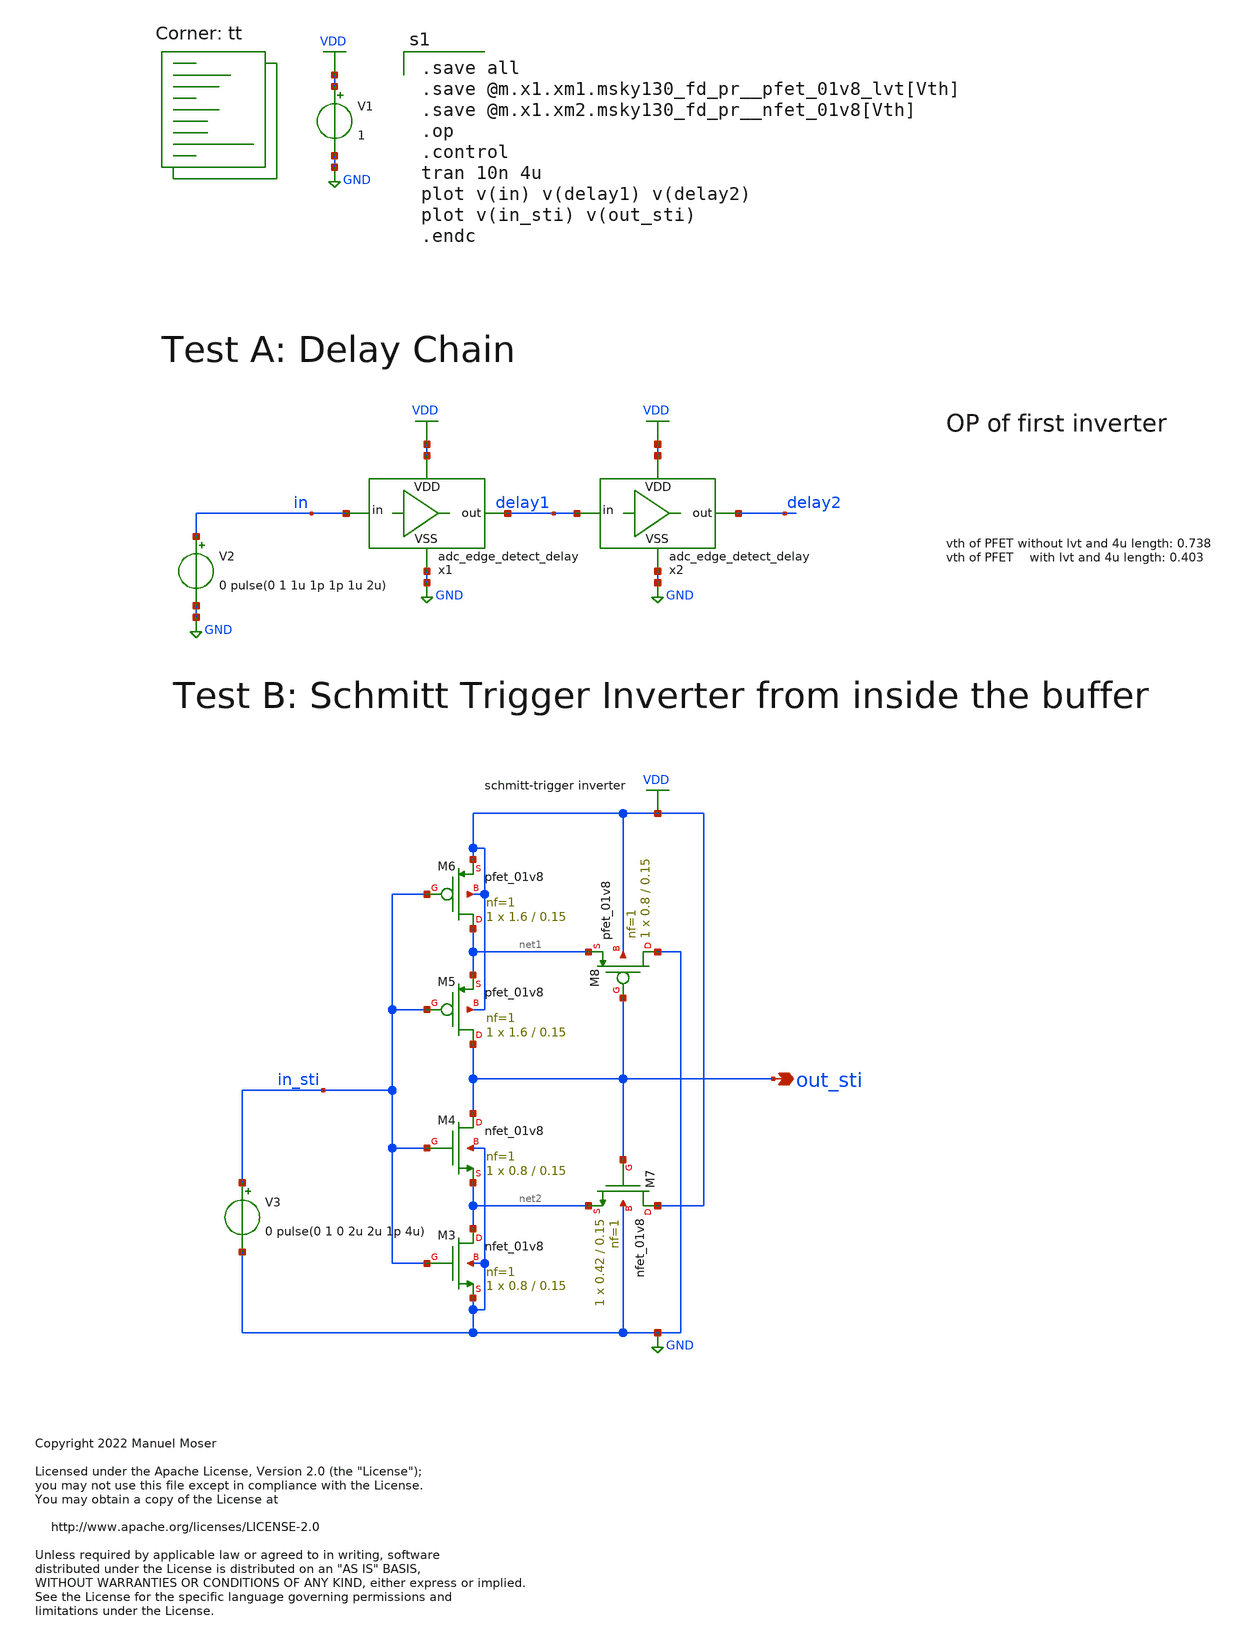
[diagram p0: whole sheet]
** sch_path: xschem/adc_edge_detect_delay/adc_edge_detect_delay_tb.sch
* Copyright 2022 Manuel Moser
* Licensed under the Apache License, Version 2.0 (the "License");
**.subckt adc_edge_detect_delay_tb out_sti
*.opin out_sti
x1 VDD in delay1 GND adc_edge_detect_delay
x2 VDD delay1 delay2 GND adc_edge_detect_delay
V1 VDD GND 1
V2 in GND 0 pulse(0 1 1u 1p 1p 1u 2u)
XM3 net2 in_sti GND GND sky130_fd_pr__nfet_01v8 L=0.15 W=0.8 nf=1 ad='int((nf+1)/2) * W/nf * 0.29' as='int((nf+2)/2) * W/nf * 0.29'
+ pd='2*int((nf+1)/2) * (W/nf + 0.29)' ps='2*int((nf+2)/2) * (W/nf + 0.29)' nrd='0.29 / W' nrs='0.29 / W'
+ sa=0 sb=0 sd=0 mult=1 m=1
XM4 out_sti in_sti net2 GND sky130_fd_pr__nfet_01v8 L=0.15 W=0.8 nf=1 ad='int((nf+1)/2) * W/nf * 0.29'
+ as='int((nf+2)/2) * W/nf * 0.29' pd='2*int((nf+1)/2) * (W/nf + 0.29)' ps='2*int((nf+2)/2) * (W/nf + 0.29)'
+ nrd='0.29 / W' nrs='0.29 / W' sa=0 sb=0 sd=0 mult=1 m=1
XM5 out_sti in_sti net1 VDD sky130_fd_pr__pfet_01v8 L=0.15 W=1.6 nf=1 ad='int((nf+1)/2) * W/nf * 0.29'
+ as='int((nf+2)/2) * W/nf * 0.29' pd='2*int((nf+1)/2) * (W/nf + 0.29)' ps='2*int((nf+2)/2) * (W/nf + 0.29)'
+ nrd='0.29 / W' nrs='0.29 / W' sa=0 sb=0 sd=0 mult=1 m=1
XM6 net1 in_sti VDD VDD sky130_fd_pr__pfet_01v8 L=0.15 W=1.6 nf=1 ad='int((nf+1)/2) * W/nf * 0.29' as='int((nf+2)/2) * W/nf * 0.29'
+ pd='2*int((nf+1)/2) * (W/nf + 0.29)' ps='2*int((nf+2)/2) * (W/nf + 0.29)' nrd='0.29 / W' nrs='0.29 / W'
+ sa=0 sb=0 sd=0 mult=1 m=1
XM7 VDD out_sti net2 GND sky130_fd_pr__nfet_01v8 L=0.15 W=0.42 nf=1 ad='int((nf+1)/2) * W/nf * 0.29'
+ as='int((nf+2)/2) * W/nf * 0.29' pd='2*int((nf+1)/2) * (W/nf + 0.29)' ps='2*int((nf+2)/2) * (W/nf + 0.29)'
+ nrd='0.29 / W' nrs='0.29 / W' sa=0 sb=0 sd=0 mult=1 m=1
XM8 GND out_sti net1 VDD sky130_fd_pr__pfet_01v8 L=0.15 W=0.8 nf=1 ad='int((nf+1)/2) * W/nf * 0.29' as='int((nf+2)/2) * W/nf * 0.29'
+ pd='2*int((nf+1)/2) * (W/nf + 0.29)' ps='2*int((nf+2)/2) * (W/nf + 0.29)' nrd='0.29 / W' nrs='0.29 / W'
+ sa=0 sb=0 sd=0 mult=1 m=1
V3 in_sti GND 0 pulse(0 1 0 2u 2u 1p 4u)
**** begin user architecture code

.save all
.save @m.x1.xm1.msky130_fd_pr__pfet_01v8_lvt[Vth]
.save @m.x1.xm2.msky130_fd_pr__nfet_01v8[Vth]
.op
.control
tran 10n 4u
plot v(in) v(delay1) v(delay2)
plot v(in_sti) v(out_sti)
.endc

.lib $::SKYWATER_MODELS/sky130.lib.spice tt
**** end user architecture code
**.ends
.GLOBAL VDD
.GLOBAL GND
.end
